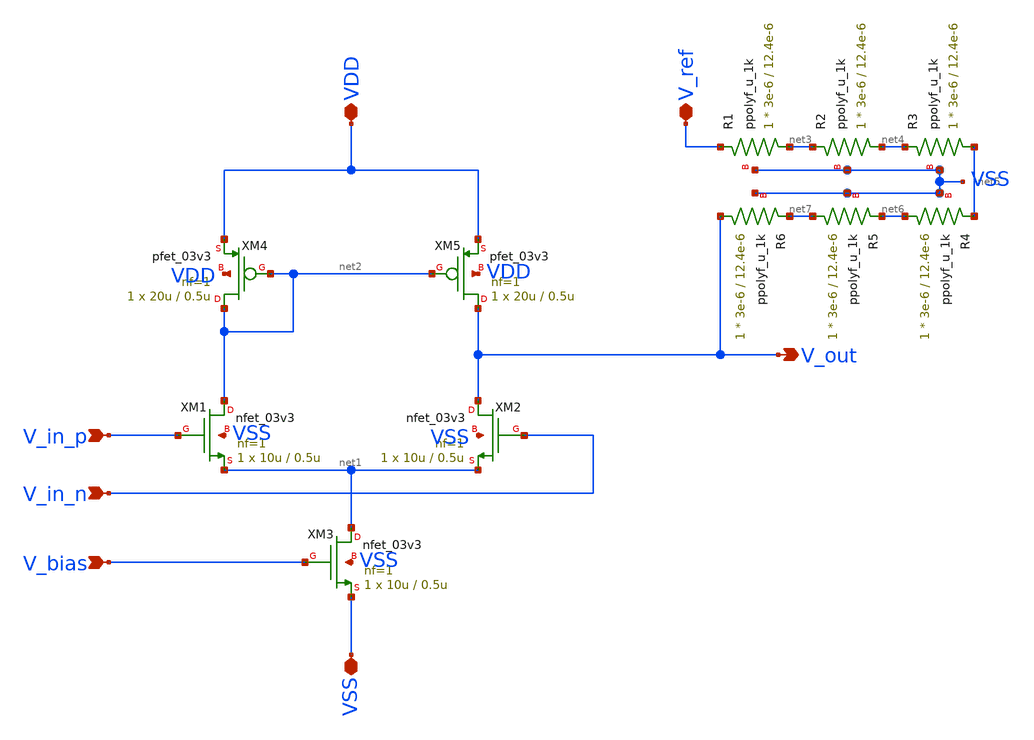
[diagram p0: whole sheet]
** sch_path: schematics/tanh_ota.sch
**.subckt tanh_ota VDD VSS V_in_p V_in_n V_bias V_out V_ref
*.iopin VDD
*.iopin VSS
*.ipin V_in_p
*.ipin V_in_n
*.ipin V_bias
*.opin V_out
*.iopin V_ref
XM1 net2 V_in_p net1 VSS nfet_03v3 L=0.5u W=10u nf=1 ad='int((nf+1)/2) * W/nf * 0.18u' as='int((nf+2)/2) * W/nf * 0.18u'
+ pd='2*int((nf+1)/2) * (W/nf + 0.18u)' ps='2*int((nf+2)/2) * (W/nf + 0.18u)' nrd='0.18u / W' nrs='0.18u / W'
+ sa=0 sb=0 sd=0 m=1
XM2 V_out V_in_n net1 VSS nfet_03v3 L=0.5u W=10u nf=1 ad='int((nf+1)/2) * W/nf * 0.18u' as='int((nf+2)/2) * W/nf * 0.18u'
+ pd='2*int((nf+1)/2) * (W/nf + 0.18u)' ps='2*int((nf+2)/2) * (W/nf + 0.18u)' nrd='0.18u / W' nrs='0.18u / W'
+ sa=0 sb=0 sd=0 m=1
XM3 net1 V_bias VSS VSS nfet_03v3 L=0.5u W=10u nf=1 ad='int((nf+1)/2) * W/nf * 0.18u' as='int((nf+2)/2) * W/nf * 0.18u'
+ pd='2*int((nf+1)/2) * (W/nf + 0.18u)' ps='2*int((nf+2)/2) * (W/nf + 0.18u)' nrd='0.18u / W' nrs='0.18u / W'
+ sa=0 sb=0 sd=0 m=1
XM4 net2 net2 VDD VDD pfet_03v3 L=0.5u W=20u nf=1 ad='int((nf+1)/2) * W/nf * 0.18u' as='int((nf+2)/2) * W/nf * 0.18u'
+ pd='2*int((nf+1)/2) * (W/nf + 0.18u)' ps='2*int((nf+2)/2) * (W/nf + 0.18u)' nrd='0.18u / W' nrs='0.18u / W'
+ sa=0 sb=0 sd=0 m=1
XM5 V_out net2 VDD VDD pfet_03v3 L=0.5u W=20u nf=1 ad='int((nf+1)/2) * W/nf * 0.18u' as='int((nf+2)/2) * W/nf * 0.18u'
+ pd='2*int((nf+1)/2) * (W/nf + 0.18u)' ps='2*int((nf+2)/2) * (W/nf + 0.18u)' nrd='0.18u / W' nrs='0.18u / W'
+ sa=0 sb=0 sd=0 m=1
XR1 net3 V_ref VSS ppolyf_u_1k r_width=3e-6 r_length=12.4e-6 m=1
XR2 net4 net3 VSS ppolyf_u_1k r_width=3e-6 r_length=12.4e-6 m=1
XR3 net5 net4 VSS ppolyf_u_1k r_width=3e-6 r_length=12.4e-6 m=1
XR4 net6 net5 VSS ppolyf_u_1k r_width=3e-6 r_length=12.4e-6 m=1
XR5 net7 net6 VSS ppolyf_u_1k r_width=3e-6 r_length=12.4e-6 m=1
XR6 V_out net7 VSS ppolyf_u_1k r_width=3e-6 r_length=12.4e-6 m=1
**.ends
.end
